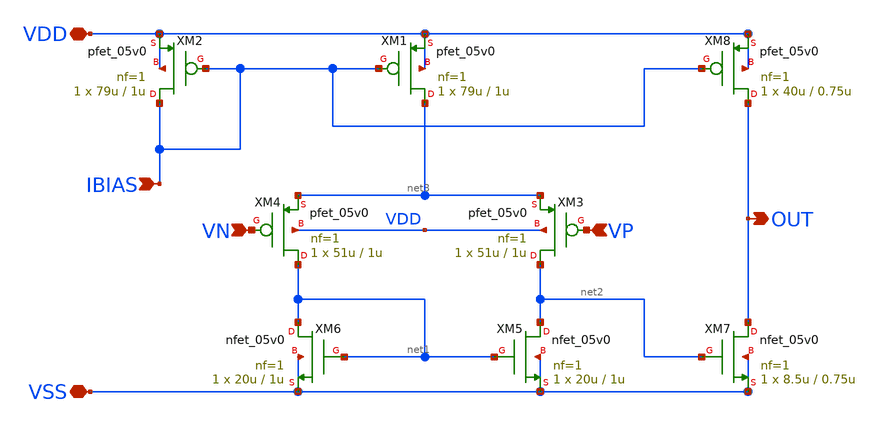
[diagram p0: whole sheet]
** sch_path: designs/pwm-comparator/pwm-comp.sch
**.subckt pwm-comp VN VP OUT VDD VSS IBIAS
*.ipin VN
*.ipin VP
*.opin OUT
*.iopin VDD
*.iopin VSS
*.ipin IBIAS
XM3 net2 VP net3 VDD pfet_05v0 L=1u W=51u nf=1 ad='int((nf+1)/2) * W/nf * 0.18u' as='int((nf+2)/2) * W/nf * 0.18u'
+ pd='2*int((nf+1)/2) * (W/nf + 0.18u)' ps='2*int((nf+2)/2) * (W/nf + 0.18u)' nrd='0.18u / W' nrs='0.18u / W'
+ sa=0 sb=0 sd=0 m=1
XM4 net1 VN net3 VDD pfet_05v0 L=1u W=51u nf=1 ad='int((nf+1)/2) * W/nf * 0.18u' as='int((nf+2)/2) * W/nf * 0.18u'
+ pd='2*int((nf+1)/2) * (W/nf + 0.18u)' ps='2*int((nf+2)/2) * (W/nf + 0.18u)' nrd='0.18u / W' nrs='0.18u / W'
+ sa=0 sb=0 sd=0 m=1
XM5 net2 net1 VSS VSS nfet_05v0 L=1u W=20u nf=1 ad='int((nf+1)/2) * W/nf * 0.18u' as='int((nf+2)/2) * W/nf * 0.18u'
+ pd='2*int((nf+1)/2) * (W/nf + 0.18u)' ps='2*int((nf+2)/2) * (W/nf + 0.18u)' nrd='0.18u / W' nrs='0.18u / W'
+ sa=0 sb=0 sd=0 m=1
XM6 net1 net1 VSS VSS nfet_05v0 L=1u W=20u nf=1 ad='int((nf+1)/2) * W/nf * 0.18u' as='int((nf+2)/2) * W/nf * 0.18u'
+ pd='2*int((nf+1)/2) * (W/nf + 0.18u)' ps='2*int((nf+2)/2) * (W/nf + 0.18u)' nrd='0.18u / W' nrs='0.18u / W'
+ sa=0 sb=0 sd=0 m=1
XM7 OUT net2 VSS VSS nfet_05v0 L=0.75u W=8.5u nf=1 ad='int((nf+1)/2) * W/nf * 0.18u' as='int((nf+2)/2) * W/nf * 0.18u'
+ pd='2*int((nf+1)/2) * (W/nf + 0.18u)' ps='2*int((nf+2)/2) * (W/nf + 0.18u)' nrd='0.18u / W' nrs='0.18u / W'
+ sa=0 sb=0 sd=0 m=1
XM8 OUT IBIAS VDD VDD pfet_05v0 L=0.75u W=40u nf=1 ad='int((nf+1)/2) * W/nf * 0.18u' as='int((nf+2)/2) * W/nf * 0.18u'
+ pd='2*int((nf+1)/2) * (W/nf + 0.18u)' ps='2*int((nf+2)/2) * (W/nf + 0.18u)' nrd='0.18u / W' nrs='0.18u / W'
+ sa=0 sb=0 sd=0 m=1
XM1 net3 IBIAS VDD VDD pfet_05v0 L=1u W=79u nf=1 ad='int((nf+1)/2) * W/nf * 0.18u' as='int((nf+2)/2) * W/nf * 0.18u'
+ pd='2*int((nf+1)/2) * (W/nf + 0.18u)' ps='2*int((nf+2)/2) * (W/nf + 0.18u)' nrd='0.18u / W' nrs='0.18u / W'
+ sa=0 sb=0 sd=0 m=1
XM2 IBIAS IBIAS VDD VDD pfet_05v0 L=1u W=79u nf=1 ad='int((nf+1)/2) * W/nf * 0.18u' as='int((nf+2)/2) * W/nf * 0.18u'
+ pd='2*int((nf+1)/2) * (W/nf + 0.18u)' ps='2*int((nf+2)/2) * (W/nf + 0.18u)' nrd='0.18u / W' nrs='0.18u / W'
+ sa=0 sb=0 sd=0 m=1
**.ends
.end
